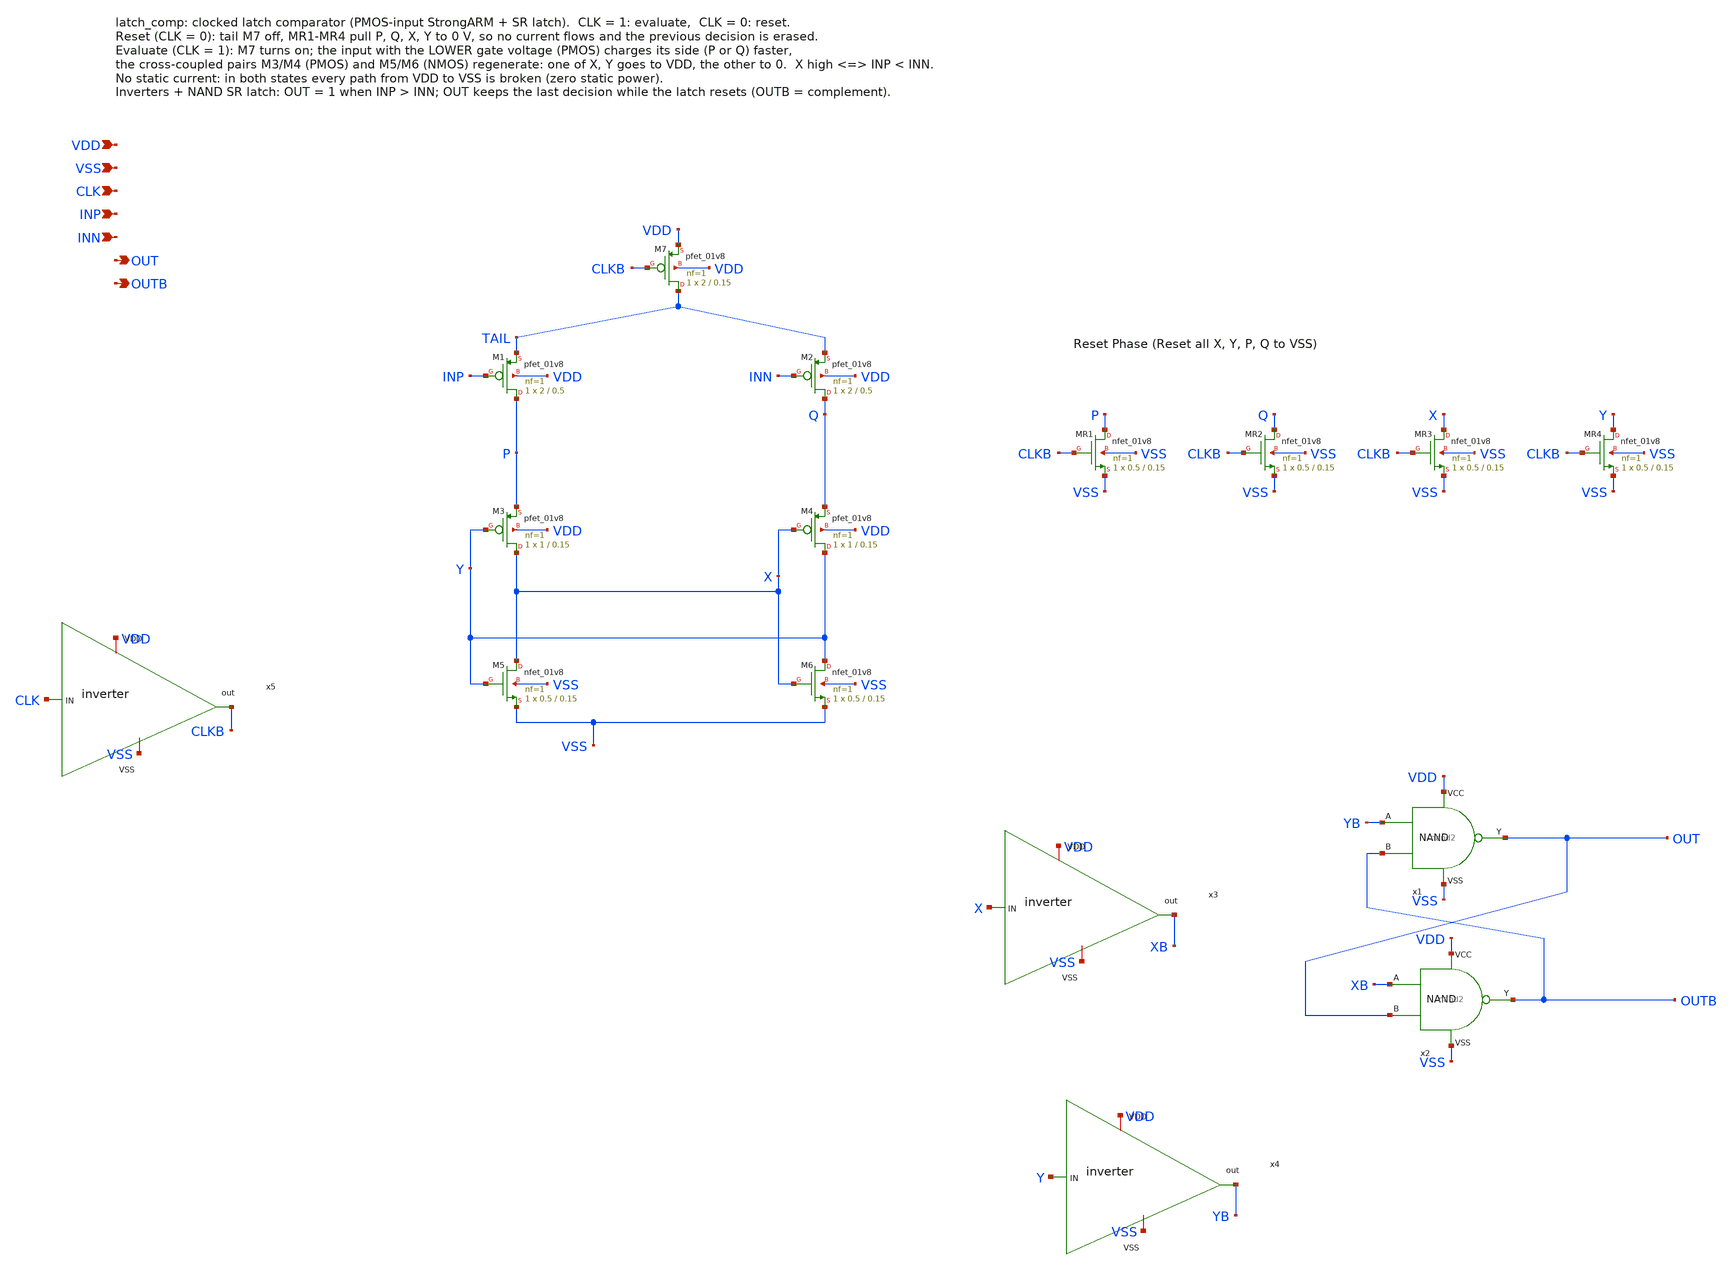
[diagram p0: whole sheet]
** sch_path: SAR_improved/latch_comp.sch
**.subckt latch_comp VDD VSS CLK INP INN OUT OUTB
*.ipin VDD
*.ipin VSS
*.ipin CLK
*.ipin INP
*.ipin INN
*.opin OUT
*.opin OUTB
XM7 TAIL CLKB VDD VDD sky130_fd_pr__pfet_01v8 L=0.15 W=2 nf=1 ad='int((nf+1)/2) * W/nf * 0.29' as='int((nf+2)/2) * W/nf * 0.29'
+ pd='2*int((nf+1)/2) * (W/nf + 0.29)' ps='2*int((nf+2)/2) * (W/nf + 0.29)' nrd='0.29 / W' nrs='0.29 / W'
+ sa=0 sb=0 sd=0 mult=1 m=1
XM1 P INP TAIL VDD sky130_fd_pr__pfet_01v8 L=0.5 W=2 nf=1 ad='int((nf+1)/2) * W/nf * 0.29' as='int((nf+2)/2) * W/nf * 0.29'
+ pd='2*int((nf+1)/2) * (W/nf + 0.29)' ps='2*int((nf+2)/2) * (W/nf + 0.29)' nrd='0.29 / W' nrs='0.29 / W'
+ sa=0 sb=0 sd=0 mult=1 m=1
XM2 Q INN TAIL VDD sky130_fd_pr__pfet_01v8 L=0.5 W=2 nf=1 ad='int((nf+1)/2) * W/nf * 0.29' as='int((nf+2)/2) * W/nf * 0.29'
+ pd='2*int((nf+1)/2) * (W/nf + 0.29)' ps='2*int((nf+2)/2) * (W/nf + 0.29)' nrd='0.29 / W' nrs='0.29 / W'
+ sa=0 sb=0 sd=0 mult=1 m=1
XM3 X Y P VDD sky130_fd_pr__pfet_01v8 L=0.15 W=1 nf=1 ad='int((nf+1)/2) * W/nf * 0.29' as='int((nf+2)/2) * W/nf * 0.29'
+ pd='2*int((nf+1)/2) * (W/nf + 0.29)' ps='2*int((nf+2)/2) * (W/nf + 0.29)' nrd='0.29 / W' nrs='0.29 / W'
+ sa=0 sb=0 sd=0 mult=1 m=1
XM4 Y X Q VDD sky130_fd_pr__pfet_01v8 L=0.15 W=1 nf=1 ad='int((nf+1)/2) * W/nf * 0.29' as='int((nf+2)/2) * W/nf * 0.29'
+ pd='2*int((nf+1)/2) * (W/nf + 0.29)' ps='2*int((nf+2)/2) * (W/nf + 0.29)' nrd='0.29 / W' nrs='0.29 / W'
+ sa=0 sb=0 sd=0 mult=1 m=1
XM5 X Y VSS VSS sky130_fd_pr__nfet_01v8 L=0.15 W=0.5 nf=1 ad='int((nf+1)/2) * W/nf * 0.29' as='int((nf+2)/2) * W/nf * 0.29'
+ pd='2*int((nf+1)/2) * (W/nf + 0.29)' ps='2*int((nf+2)/2) * (W/nf + 0.29)' nrd='0.29 / W' nrs='0.29 / W'
+ sa=0 sb=0 sd=0 mult=1 m=1
XM6 Y X VSS VSS sky130_fd_pr__nfet_01v8 L=0.15 W=0.5 nf=1 ad='int((nf+1)/2) * W/nf * 0.29' as='int((nf+2)/2) * W/nf * 0.29'
+ pd='2*int((nf+1)/2) * (W/nf + 0.29)' ps='2*int((nf+2)/2) * (W/nf + 0.29)' nrd='0.29 / W' nrs='0.29 / W'
+ sa=0 sb=0 sd=0 mult=1 m=1
XMR1 P CLKB VSS VSS sky130_fd_pr__nfet_01v8 L=0.15 W=0.5 nf=1 ad='int((nf+1)/2) * W/nf * 0.29' as='int((nf+2)/2) * W/nf * 0.29'
+ pd='2*int((nf+1)/2) * (W/nf + 0.29)' ps='2*int((nf+2)/2) * (W/nf + 0.29)' nrd='0.29 / W' nrs='0.29 / W'
+ sa=0 sb=0 sd=0 mult=1 m=1
XMR2 Q CLKB VSS VSS sky130_fd_pr__nfet_01v8 L=0.15 W=0.5 nf=1 ad='int((nf+1)/2) * W/nf * 0.29' as='int((nf+2)/2) * W/nf * 0.29'
+ pd='2*int((nf+1)/2) * (W/nf + 0.29)' ps='2*int((nf+2)/2) * (W/nf + 0.29)' nrd='0.29 / W' nrs='0.29 / W'
+ sa=0 sb=0 sd=0 mult=1 m=1
XMR3 X CLKB VSS VSS sky130_fd_pr__nfet_01v8 L=0.15 W=0.5 nf=1 ad='int((nf+1)/2) * W/nf * 0.29' as='int((nf+2)/2) * W/nf * 0.29'
+ pd='2*int((nf+1)/2) * (W/nf + 0.29)' ps='2*int((nf+2)/2) * (W/nf + 0.29)' nrd='0.29 / W' nrs='0.29 / W'
+ sa=0 sb=0 sd=0 mult=1 m=1
XMR4 Y CLKB VSS VSS sky130_fd_pr__nfet_01v8 L=0.15 W=0.5 nf=1 ad='int((nf+1)/2) * W/nf * 0.29' as='int((nf+2)/2) * W/nf * 0.29'
+ pd='2*int((nf+1)/2) * (W/nf + 0.29)' ps='2*int((nf+2)/2) * (W/nf + 0.29)' nrd='0.29 / W' nrs='0.29 / W'
+ sa=0 sb=0 sd=0 mult=1 m=1
x1 YB OUTB OUT VDD VSS nand2
x2 XB OUT OUTB VDD VSS nand2
x3 VDD X XB VSS inverter
x4 VDD Y YB VSS inverter
x5 VDD CLK CLKB VSS inverter
**.ends

* expanding   symbol:  /home/ttuser/Documents/ADCAnalogDesign/nand2.sym # of pins=5
** sym_path: SAR_improved/nand2.sym
** sch_path: SAR_improved/nand2.sch
.subckt nand2 A B Y VCC VSS
*.ipin A
*.ipin B
*.opin Y
*.iopin VCC
*.iopin VSS
XM1 Y A VCC VCC sky130_fd_pr__pfet_01v8 L=0.15 W=2 nf=1 ad='int((nf+1)/2) * W/nf * 0.29' as='int((nf+2)/2) * W/nf * 0.29'
+ pd='2*int((nf+1)/2) * (W/nf + 0.29)' ps='2*int((nf+2)/2) * (W/nf + 0.29)' nrd='0.29 / W' nrs='0.29 / W'
+ sa=0 sb=0 sd=0 mult=1 m=1
XM2 Y B VCC VCC sky130_fd_pr__pfet_01v8 L=0.15 W=2 nf=1 ad='int((nf+1)/2) * W/nf * 0.29' as='int((nf+2)/2) * W/nf * 0.29'
+ pd='2*int((nf+1)/2) * (W/nf + 0.29)' ps='2*int((nf+2)/2) * (W/nf + 0.29)' nrd='0.29 / W' nrs='0.29 / W'
+ sa=0 sb=0 sd=0 mult=1 m=1
XM3 Y A N1 VSS sky130_fd_pr__nfet_01v8 L=0.15 W=2 nf=1 ad='int((nf+1)/2) * W/nf * 0.29' as='int((nf+2)/2) * W/nf * 0.29'
+ pd='2*int((nf+1)/2) * (W/nf + 0.29)' ps='2*int((nf+2)/2) * (W/nf + 0.29)' nrd='0.29 / W' nrs='0.29 / W'
+ sa=0 sb=0 sd=0 mult=1 m=1
XM4 N1 B VSS VSS sky130_fd_pr__nfet_01v8 L=0.15 W=2 nf=1 ad='int((nf+1)/2) * W/nf * 0.29' as='int((nf+2)/2) * W/nf * 0.29'
+ pd='2*int((nf+1)/2) * (W/nf + 0.29)' ps='2*int((nf+2)/2) * (W/nf + 0.29)' nrd='0.29 / W' nrs='0.29 / W'
+ sa=0 sb=0 sd=0 mult=1 m=1
.ends


* expanding   symbol:  /home/ttuser/Documents/ADCAnalogDesign/inverter.sym # of pins=4
** sym_path: SAR_improved/inverter.sym
** sch_path: SAR_improved/inverter.sch
.subckt inverter VDD IN out VSS
*.ipin IN
*.opin out
*.iopin VDD
*.iopin VSS
XM3 out IN VDD VDD sky130_fd_pr__pfet_01v8 L=0.15 W=1 nf=1 ad='int((nf+1)/2) * W/nf * 0.29' as='int((nf+2)/2) * W/nf * 0.29'
+ pd='2*int((nf+1)/2) * (W/nf + 0.29)' ps='2*int((nf+2)/2) * (W/nf + 0.29)' nrd='0.29 / W' nrs='0.29 / W'
+ sa=0 sb=0 sd=0 mult=1 m=1
XM2 out IN VSS VSS sky130_fd_pr__nfet_01v8 L=0.15 W=1 nf=1 ad='int((nf+1)/2) * W/nf * 0.29' as='int((nf+2)/2) * W/nf * 0.29'
+ pd='2*int((nf+1)/2) * (W/nf + 0.29)' ps='2*int((nf+2)/2) * (W/nf + 0.29)' nrd='0.29 / W' nrs='0.29 / W'
+ sa=0 sb=0 sd=0 mult=1 m=1
.ends

.end
